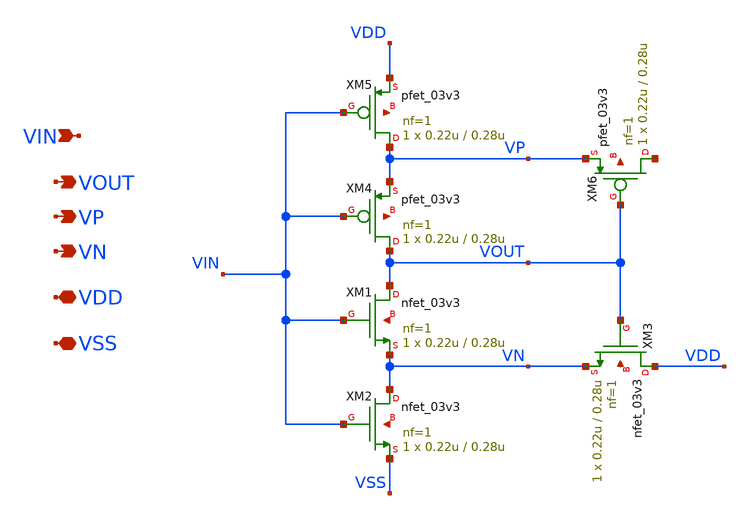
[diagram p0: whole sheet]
** sch_path: analog/schmitt_trigger_comparator/comparator.sch
**.subckt comparator VIN VOUT VDD VSS VN VP
*.ipin VIN
*.opin VOUT
*.iopin VDD
*.iopin VSS
*.opin VN
*.opin VP
XM1 VOUT VIN VN net1 nfet_03v3 L=0.28u W=0.22u nf=1 ad='int((nf+1)/2) * W/nf * 0.18u' as='int((nf+2)/2) * W/nf * 0.18u'
+ pd='2*int((nf+1)/2) * (W/nf + 0.18u)' ps='2*int((nf+2)/2) * (W/nf + 0.18u)' nrd='0.18u / W' nrs='0.18u / W'
+ sa=0 sb=0 sd=0 m=1
XM2 VN VIN VSS net2 nfet_03v3 L=0.28u W=0.22u nf=1 ad='int((nf+1)/2) * W/nf * 0.18u' as='int((nf+2)/2) * W/nf * 0.18u'
+ pd='2*int((nf+1)/2) * (W/nf + 0.18u)' ps='2*int((nf+2)/2) * (W/nf + 0.18u)' nrd='0.18u / W' nrs='0.18u / W'
+ sa=0 sb=0 sd=0 m=1
XM3 VDD VOUT VN net3 nfet_03v3 L=0.28u W=0.22u nf=1 ad='int((nf+1)/2) * W/nf * 0.18u' as='int((nf+2)/2) * W/nf * 0.18u'
+ pd='2*int((nf+1)/2) * (W/nf + 0.18u)' ps='2*int((nf+2)/2) * (W/nf + 0.18u)' nrd='0.18u / W' nrs='0.18u / W'
+ sa=0 sb=0 sd=0 m=1
XM4 VOUT VIN VP net4 pfet_03v3 L=0.28u W=0.22u nf=1 ad='int((nf+1)/2) * W/nf * 0.18u' as='int((nf+2)/2) * W/nf * 0.18u'
+ pd='2*int((nf+1)/2) * (W/nf + 0.18u)' ps='2*int((nf+2)/2) * (W/nf + 0.18u)' nrd='0.18u / W' nrs='0.18u / W'
+ sa=0 sb=0 sd=0 m=1
XM5 VP VIN VDD net5 pfet_03v3 L=0.28u W=0.22u nf=1 ad='int((nf+1)/2) * W/nf * 0.18u' as='int((nf+2)/2) * W/nf * 0.18u'
+ pd='2*int((nf+1)/2) * (W/nf + 0.18u)' ps='2*int((nf+2)/2) * (W/nf + 0.18u)' nrd='0.18u / W' nrs='0.18u / W'
+ sa=0 sb=0 sd=0 m=1
XM6 net6 VOUT VP net7 pfet_03v3 L=0.28u W=0.22u nf=1 ad='int((nf+1)/2) * W/nf * 0.18u' as='int((nf+2)/2) * W/nf * 0.18u'
+ pd='2*int((nf+1)/2) * (W/nf + 0.18u)' ps='2*int((nf+2)/2) * (W/nf + 0.18u)' nrd='0.18u / W' nrs='0.18u / W'
+ sa=0 sb=0 sd=0 m=1
**.ends
.end
